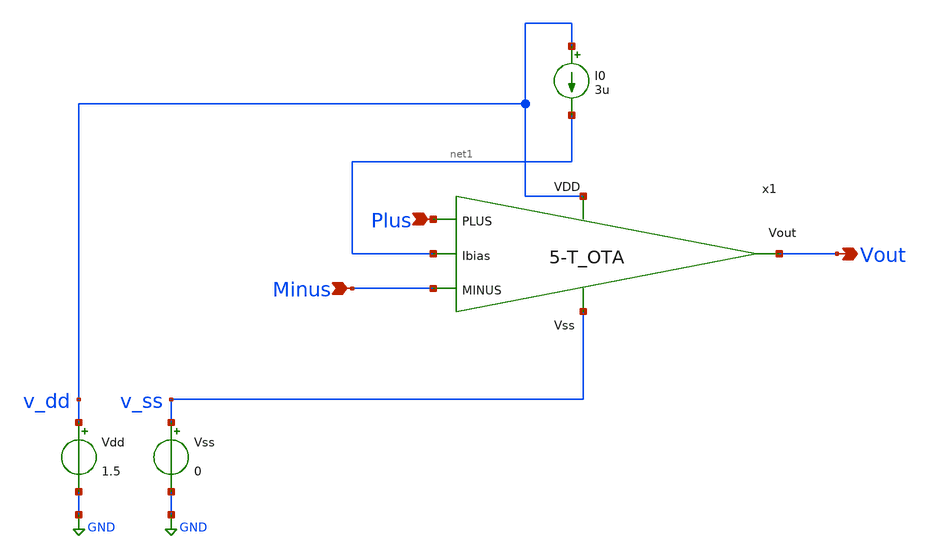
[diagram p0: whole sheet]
** sch_path: DSM/Schematics/IC_Designs_Hrishi/RealCircuits/VCCS_5tOTA.sch
* DSM/Schematics/Designs_Hrishi/RealCircuits/5-T_OTA/5-T_OTA.sch:
* (c) 2024 Hrishikesh, @HSB
**.subckt VCCS_5tOTA Minus Vout Plus
*.ipin Minus
*.opin Vout
*.ipin Plus
Vdd v_dd GND 1.5
Vss v_ss GND 0
I0 v_dd net1 3u
x1 v_dd net1 Vout Plus Minus v_ss 5-T_OTA
**.ends

* expanding   symbol:
*+  /foss/designs/CEMS_DSM/DSM/Schematics/IC_Designs_Hrishi/RealCircuits/5-T_OTA/5-T_OTA.sym # of pins=6
** sym_path: DSM/Schematics/Designs_Hrishi/RealCircuits/5-T_OTA/5-T_OTA.sym
** sch_path: DSM/Schematics/Designs_Hrishi/RealCircuits/5-T_OTA/5-T_OTA.sch
.subckt 5-T_OTA VDD Ibias Vout PLUS MINUS Vss
*.ipin MINUS
*.ipin PLUS
*.ipin VDD
*.ipin Ibias
*.ipin Vss
*.opin Vout
XM10 Vout net1 VDD VDD sg13_lv_pmos w=0.136u l=0.5u ng=1 m=1 mm_ok=1
XM11 net1 net1 VDD VDD sg13_lv_pmos w=0.136u l=0.5u ng=1 m=1 mm_ok=1
XM12 net1 PLUS net2 Vss sg13_lv_nmos w=0.15u l=2u ng=1 m=1 mm_ok=1
XM13 Vout MINUS net2 Vss sg13_lv_nmos w=0.15u l=2u ng=1 m=1 mm_ok=1
XM14 net2 net4 Vss Vss sg13_lv_nmos w=0.30u l=2u ng=1 m=1 mm_ok=1
XM1 net3 net4 Vss Vss sg13_lv_nmos w=0.15u l=2u ng=1 m=1 mm_ok=1
XM2 VDD VDD net3 Vss sg13_lv_nmos w=0.15u l=2u ng=1 m=1 mm_ok=1
XM3 net4 net4 Vss Vss sg13_lv_nmos w=0.15u l=2u ng=1 m=1 mm_ok=1
XM4 Ibias VDD net4 Vss sg13_lv_nmos w=0.15u l=2u ng=1 m=1 mm_ok=1
.ends

.GLOBAL GND
.end
